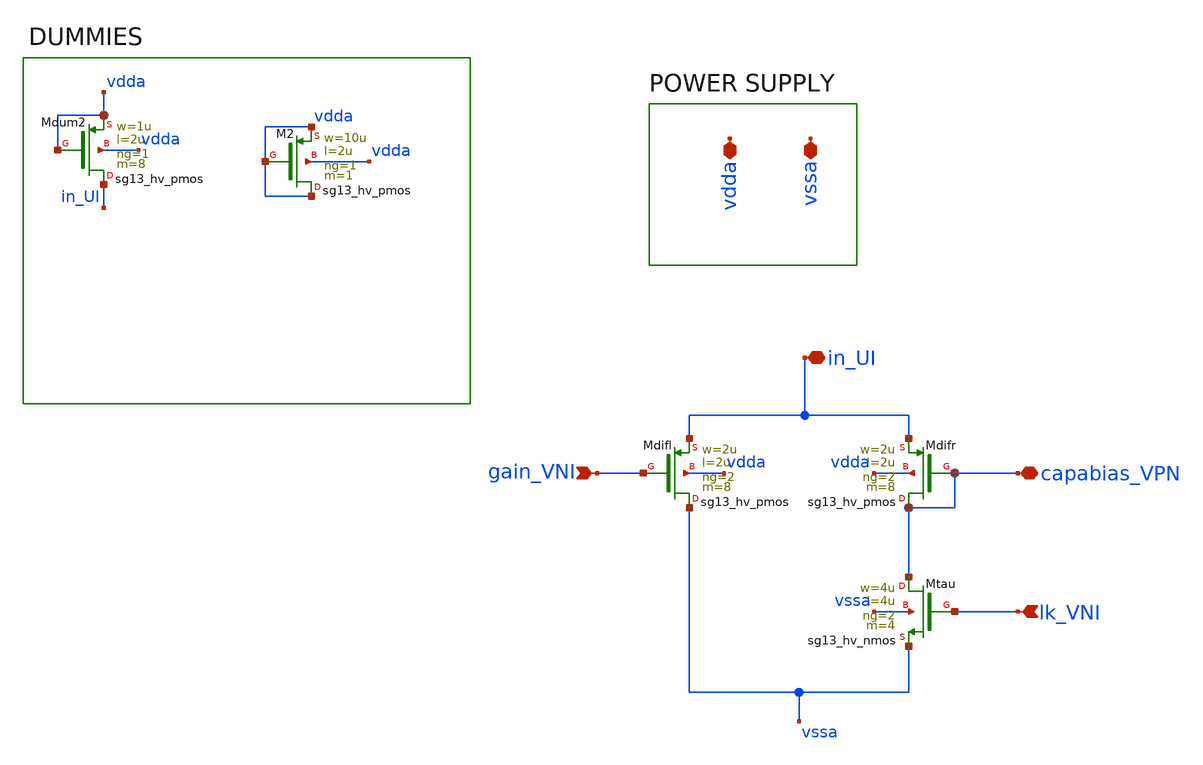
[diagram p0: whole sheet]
** sch_path: DPI_gain.sch
**.subckt DPI_gain gain_VNI lk_VNI capabias_VPN vssa vdda in_UI
*.ipin gain_VNI
*.ipin lk_VNI
*.iopin capabias_VPN
*.iopin vssa
*.iopin vdda
*.iopin in_UI
XMdifl vssa gain_VNI in_UI vdda sg13_hv_pmos w=2u l=2u ng=2 m=8 mm_ok=1
XMdifr capabias_VPN capabias_VPN in_UI vdda sg13_hv_pmos w=2u l=2u ng=2 m=8 mm_ok=1
XMtau capabias_VPN lk_VNI vssa vssa sg13_hv_nmos w=4u l=4u ng=2 m=4 mm_ok=1
XMdum2 in_UI vdda vdda vdda sg13_hv_pmos w=1u l=2u ng=1 m=8 mm_ok=1
XM2 vdda vdda vdda vdda sg13_hv_pmos w=10u l=2u ng=1 m=1 mm_ok=1
**.ends
.end
